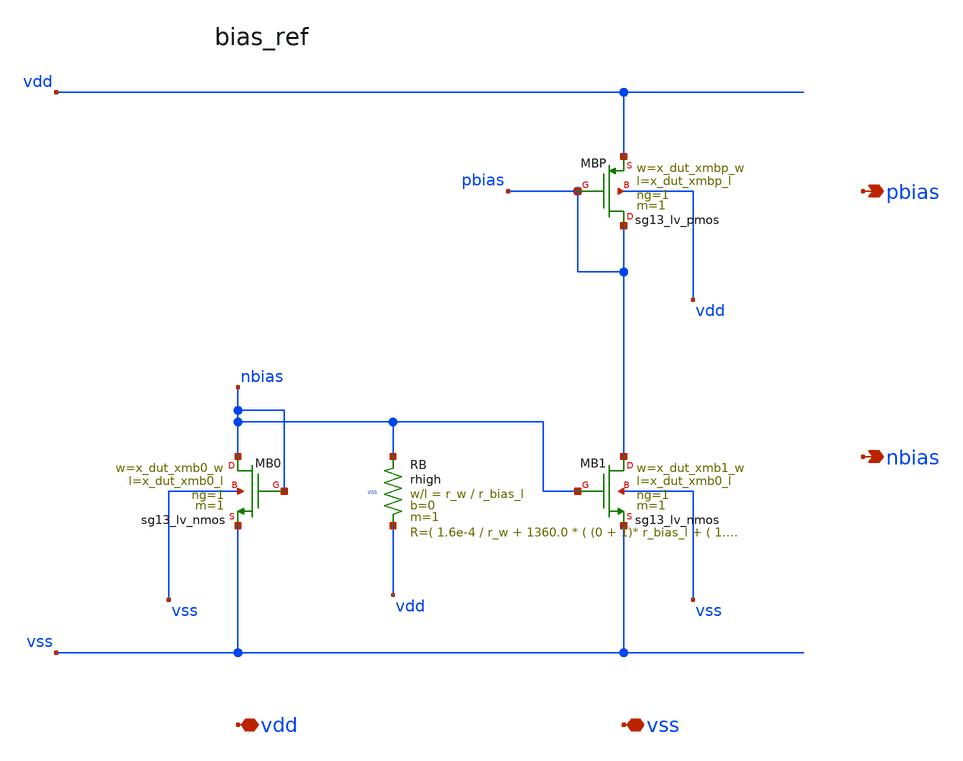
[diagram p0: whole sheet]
** sch_path: circuits/ldo_ihp_capless/xschem/blocks/bias_ref.sch
**.subckt bias_ref vdd vss pbias nbias
*.iopin vdd
*.iopin vss
*.opin pbias
*.opin nbias
XRB nbias vdd vss rhigh w=r_w l=r_bias_l m=1 b=0 mm_ok=1
XMB0 nbias nbias vss vss sg13_lv_nmos w=x_dut_xmb0_w l=x_dut_xmb0_l ng=1 m=1 mm_ok=1
XMB1 pbias nbias vss vss sg13_lv_nmos w=x_dut_xmb1_w l=x_dut_xmb0_l ng=1 m=1 mm_ok=1
XMBP pbias pbias vdd vdd sg13_lv_pmos w=x_dut_xmbp_w l=x_dut_xmbp_l ng=1 m=1 mm_ok=1
**.ends
.end
